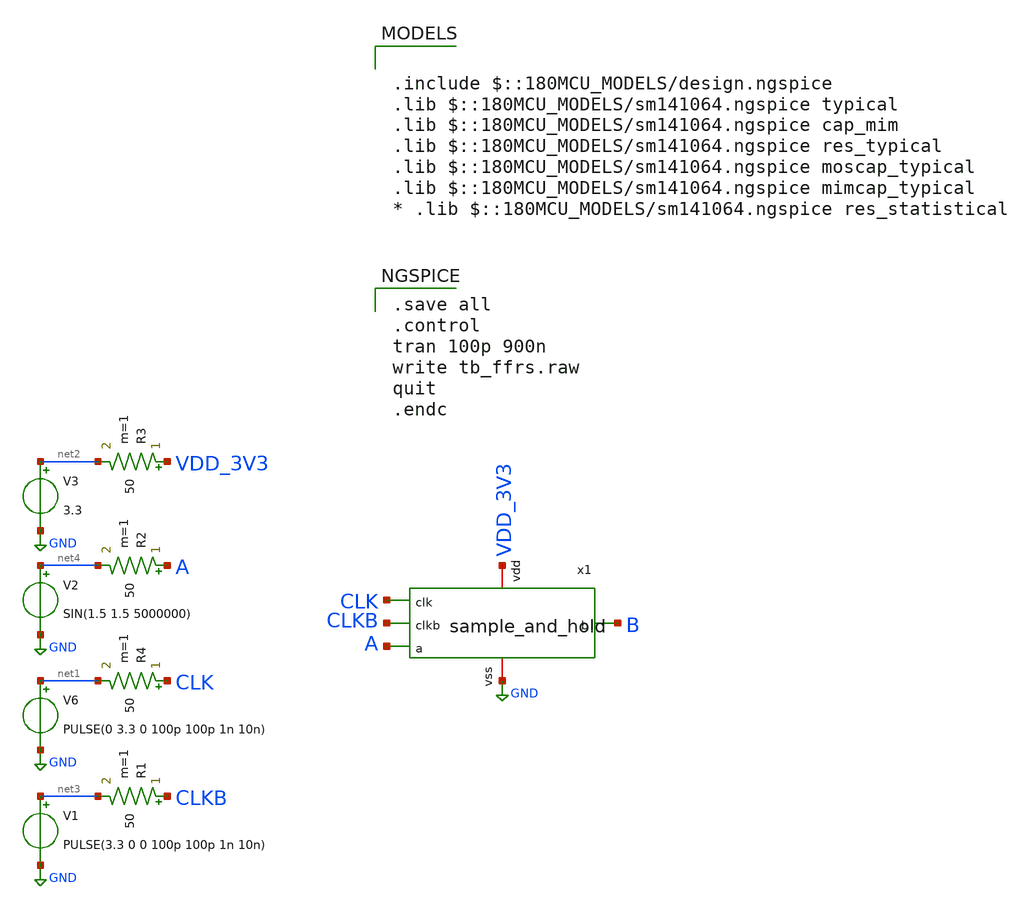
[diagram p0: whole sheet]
** sch_path: designs/libs/sample_and_hold/sample_and_hold_tb.sch
**.subckt sample_and_hold_tb
V6 net1 GND PULSE(0 3.3 0 100p 100p 1n 10n)
R4 CLK net1 50 m=1
V3 net2 GND 3.3
R3 VDD_3V3 net2 50 m=1
x1 VDD_3V3 GND CLK CLKB A B sample_and_hold
V1 net3 GND PULSE(3.3 0 0 100p 100p 1n 10n)
R1 CLKB net3 50 m=1
V2 net4 GND SIN(1.5 1.5 5000000)
R2 A net4 50 m=1
**** begin user architecture code

.include $::180MCU_MODELS/design.ngspice
.lib $::180MCU_MODELS/sm141064.ngspice typical
.lib $::180MCU_MODELS/sm141064.ngspice cap_mim
.lib $::180MCU_MODELS/sm141064.ngspice res_typical
.lib $::180MCU_MODELS/sm141064.ngspice moscap_typical
.lib $::180MCU_MODELS/sm141064.ngspice mimcap_typical
* .lib $::180MCU_MODELS/sm141064.ngspice res_statistical


.save all
.control
tran 100p 900n
write tb_ffrs.raw
quit
.endc

**** end user architecture code
**.ends

* expanding   symbol:  libs/sample_and_hold/sample_and_hold.sym # of pins=6
** sym_path: designs/libs/sample_and_hold/sample_and_hold.sym
** sch_path: designs/libs/sample_and_hold/sample_and_hold.sch
.subckt sample_and_hold vdd vss clk clkb a b
*.iopin vdd
*.iopin vss
*.ipin clk
*.ipin clkb
*.ipin a
*.opin b
XM1 a clk net1 vss nfet_03v3 L=0.28u W=0.22u nf=1 ad='int((nf+1)/2) * W/nf * 0.18u' as='int((nf+2)/2) * W/nf * 0.18u'
+ pd='2*int((nf+1)/2) * (W/nf + 0.18u)' ps='2*int((nf+2)/2) * (W/nf + 0.18u)' nrd='0.18u / W' nrs='0.18u / W'
+ sa=0 sb=0 sd=0 m=1
XM2 net3 clkb net2 net2 pfet_03v3 L=0.28u W=0.22u nf=1 ad='int((nf+1)/2) * W/nf * 0.18u' as='int((nf+2)/2) * W/nf * 0.18u'
+ pd='2*int((nf+1)/2) * (W/nf + 0.18u)' ps='2*int((nf+2)/2) * (W/nf + 0.18u)' nrd='0.18u / W' nrs='0.18u / W'
+ sa=0 sb=0 sd=0 m=1
XM3 vss clkb net1 vss nfet_03v3 L=0.28u W=0.22u nf=1 ad='int((nf+1)/2) * W/nf * 0.18u' as='int((nf+2)/2) * W/nf * 0.18u'
+ pd='2*int((nf+1)/2) * (W/nf + 0.18u)' ps='2*int((nf+2)/2) * (W/nf + 0.18u)' nrd='0.18u / W' nrs='0.18u / W'
+ sa=0 sb=0 sd=0 m=1
XM4 vdd net3 net2 net2 pfet_03v3 L=0.28u W=0.22u nf=1 ad='int((nf+1)/2) * W/nf * 0.18u' as='int((nf+2)/2) * W/nf * 0.18u'
+ pd='2*int((nf+1)/2) * (W/nf + 0.18u)' ps='2*int((nf+2)/2) * (W/nf + 0.18u)' nrd='0.18u / W' nrs='0.18u / W'
+ sa=0 sb=0 sd=0 m=1
XM5 net4 vdd net3 vss nfet_03v3 L=0.28u W=0.22u nf=1 ad='int((nf+1)/2) * W/nf * 0.18u' as='int((nf+2)/2) * W/nf * 0.18u'
+ pd='2*int((nf+1)/2) * (W/nf + 0.18u)' ps='2*int((nf+2)/2) * (W/nf + 0.18u)' nrd='0.18u / W' nrs='0.18u / W'
+ sa=0 sb=0 sd=0 m=1
XM6 vss clkb net4 vss nfet_03v3 L=0.28u W=0.22u nf=1 ad='int((nf+1)/2) * W/nf * 0.18u' as='int((nf+2)/2) * W/nf * 0.18u'
+ pd='2*int((nf+1)/2) * (W/nf + 0.18u)' ps='2*int((nf+2)/2) * (W/nf + 0.18u)' nrd='0.18u / W' nrs='0.18u / W'
+ sa=0 sb=0 sd=0 m=1
XM7 b net3 a vss nfet_03v3 L=0.28u W=0.22u nf=1 ad='int((nf+1)/2) * W/nf * 0.18u' as='int((nf+2)/2) * W/nf * 0.18u'
+ pd='2*int((nf+1)/2) * (W/nf + 0.18u)' ps='2*int((nf+2)/2) * (W/nf + 0.18u)' nrd='0.18u / W' nrs='0.18u / W'
+ sa=0 sb=0 sd=0 m=1
XM8 b clkb a vdd pfet_03v3 L=0.28u W=0.22u nf=1 ad='int((nf+1)/2) * W/nf * 0.18u' as='int((nf+2)/2) * W/nf * 0.18u'
+ pd='2*int((nf+1)/2) * (W/nf + 0.18u)' ps='2*int((nf+2)/2) * (W/nf + 0.18u)' nrd='0.18u / W' nrs='0.18u / W'
+ sa=0 sb=0 sd=0 m=1
XC1 net2 net1 cap_mim_1f0fF c_width=1e-6 c_length=1e-6 m=1
.ends

.GLOBAL GND
.end
